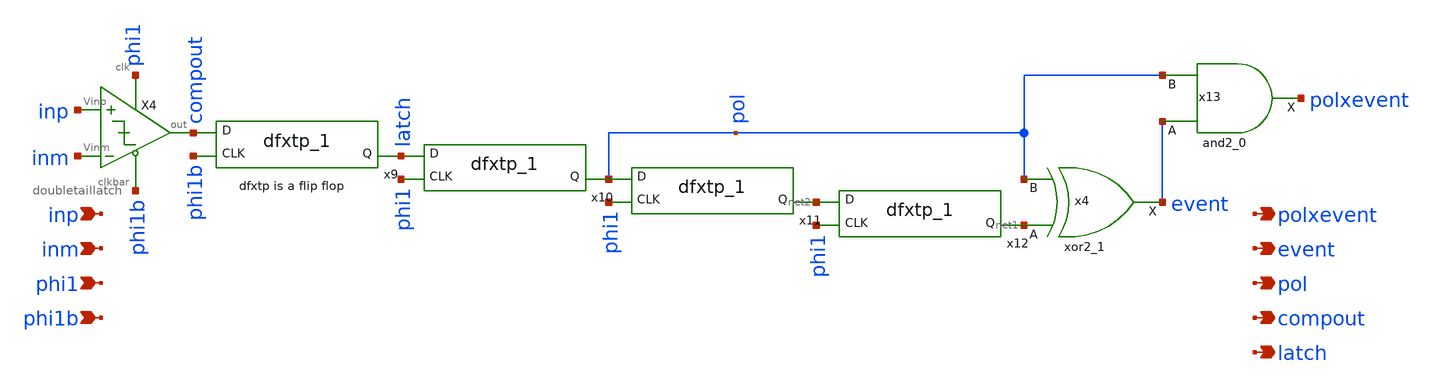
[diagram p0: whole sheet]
** sch_path: xschem/comparator/comparator_out.sch
**.subckt comparator_out inp event polxevent pol inm phi1 phi1b compout latch
*.ipin inp
*.opin event
*.opin polxevent
*.opin pol
*.ipin inm
*.ipin phi1
*.ipin phi1b
*.opin compout
*.opin latch
X4 inp inm compout phi1 phi1b doubletaillatch
x4 net1 pol GND GND VDD VDD event sky130_fd_sc_lp__xor2_1
x11 phi1 pol gnd gnd vdd vdd net2 sky130_fd_sc_lp__dfxtp_1
x12 phi1 net2 gnd gnd vdd vdd net1 sky130_fd_sc_lp__dfxtp_1
x9 phi1b compout gnd gnd vdd vdd latch sky130_fd_sc_lp__dfxtp_1
x10 phi1 latch gnd gnd vdd vdd pol sky130_fd_sc_lp__dfxtp_1
x13 event pol GND GND VDD VDD polxevent sky130_fd_sc_lp__and2_0
**.ends

* expanding   symbol:  comparator/doubletaillatch.sym # of pins=5
** sym_path: xschem/comparator/doubletaillatch.sym
** sch_path: xschem/comparator/doubletaillatch.sch
.subckt doubletaillatch Vinp Vinm out clk clkbar
*.ipin clkbar
*.opin out
*.ipin Vinp
*.ipin Vinm
*.ipin clk
XM3 rightSD out VDD VDD sky130_fd_pr__pfet_01v8 L=0.18 W=0.42 nf=1 ad='int((nf+1)/2) * W/nf * 0.29' as='int((nf+2)/2) * W/nf * 0.29'
+ pd='2*int((nf+1)/2) * (W/nf + 0.29)' ps='2*int((nf+2)/2) * (W/nf + 0.29)' nrd='0.29 / W' nrs='0.29 / W'
+ sa=0 sb=0 sd=0 mult=1 m=1
XM4 out2 rightGSD rightSD VDD sky130_fd_pr__pfet_01v8 L=0.18 W=0.42 nf=1 ad='int((nf+1)/2) * W/nf * 0.29'
+ as='int((nf+2)/2) * W/nf * 0.29' pd='2*int((nf+1)/2) * (W/nf + 0.29)' ps='2*int((nf+2)/2) * (W/nf + 0.29)'
+ nrd='0.29 / W' nrs='0.29 / W' sa=0 sb=0 sd=0 mult=1 m=1
XM5 VDD out2 leftSD VDD sky130_fd_pr__pfet_01v8 L=0.18 W=0.42 nf=1 ad='int((nf+1)/2) * W/nf * 0.29' as='int((nf+2)/2) * W/nf * 0.29'
+ pd='2*int((nf+1)/2) * (W/nf + 0.29)' ps='2*int((nf+2)/2) * (W/nf + 0.29)' nrd='0.29 / W' nrs='0.29 / W'
+ sa=0 sb=0 sd=0 mult=1 m=1
XM6 leftSD leftGD out VDD sky130_fd_pr__pfet_01v8 L=0.18 W=0.42 nf=1 ad='int((nf+1)/2) * W/nf * 0.29'
+ as='int((nf+2)/2) * W/nf * 0.29' pd='2*int((nf+1)/2) * (W/nf + 0.29)' ps='2*int((nf+2)/2) * (W/nf + 0.29)'
+ nrd='0.29 / W' nrs='0.29 / W' sa=0 sb=0 sd=0 mult=1 m=1
XM11 VDD clk rightGSD VDD sky130_fd_pr__pfet_01v8 L=0.18 W=0.42 nf=1 ad='int((nf+1)/2) * W/nf * 0.29'
+ as='int((nf+2)/2) * W/nf * 0.29' pd='2*int((nf+1)/2) * (W/nf + 0.29)' ps='2*int((nf+2)/2) * (W/nf + 0.29)'
+ nrd='0.29 / W' nrs='0.29 / W' sa=0 sb=0 sd=0 mult=1 m=1
XM12 leftGD clk VDD VDD sky130_fd_pr__pfet_01v8 L=0.18 W=0.42 nf=1 ad='int((nf+1)/2) * W/nf * 0.29' as='int((nf+2)/2) * W/nf * 0.29'
+ pd='2*int((nf+1)/2) * (W/nf + 0.29)' ps='2*int((nf+2)/2) * (W/nf + 0.29)' nrd='0.29 / W' nrs='0.29 / W'
+ sa=0 sb=0 sd=0 mult=1 m=1
XM7 out clkbar GND GND sky130_fd_pr__nfet_01v8 L=0.18 W=0.42 nf=1 ad='int((nf+1)/2) * W/nf * 0.29' as='int((nf+2)/2) * W/nf * 0.29'
+ pd='2*int((nf+1)/2) * (W/nf + 0.29)' ps='2*int((nf+2)/2) * (W/nf + 0.29)' nrd='0.29 / W' nrs='0.29 / W'
+ sa=0 sb=0 sd=0 mult=1 m=1
XM8 out2 out GND GND sky130_fd_pr__nfet_01v8 L=0.18 W=0.42 nf=1 ad='int((nf+1)/2) * W/nf * 0.29' as='int((nf+2)/2) * W/nf * 0.29'
+ pd='2*int((nf+1)/2) * (W/nf + 0.29)' ps='2*int((nf+2)/2) * (W/nf + 0.29)' nrd='0.29 / W' nrs='0.29 / W'
+ sa=0 sb=0 sd=0 mult=1 m=1
XM9 GND clkbar out2 GND sky130_fd_pr__nfet_01v8 L=0.18 W=0.42 nf=1 ad='int((nf+1)/2) * W/nf * 0.29' as='int((nf+2)/2) * W/nf * 0.29'
+ pd='2*int((nf+1)/2) * (W/nf + 0.29)' ps='2*int((nf+2)/2) * (W/nf + 0.29)' nrd='0.29 / W' nrs='0.29 / W'
+ sa=0 sb=0 sd=0 mult=1 m=1
XM10 GND out2 out GND sky130_fd_pr__nfet_01v8 L=0.18 W=0.42 nf=1 ad='int((nf+1)/2) * W/nf * 0.29' as='int((nf+2)/2) * W/nf * 0.29'
+ pd='2*int((nf+1)/2) * (W/nf + 0.29)' ps='2*int((nf+2)/2) * (W/nf + 0.29)' nrd='0.29 / W' nrs='0.29 / W'
+ sa=0 sb=0 sd=0 mult=1 m=1
XM13 leftGD Vinp rem GND sky130_fd_pr__nfet_01v8 L=0.18 W=0.42 nf=1 ad='int((nf+1)/2) * W/nf * 0.29'
+ as='int((nf+2)/2) * W/nf * 0.29' pd='2*int((nf+1)/2) * (W/nf + 0.29)' ps='2*int((nf+2)/2) * (W/nf + 0.29)'
+ nrd='0.29 / W' nrs='0.29 / W' sa=0 sb=0 sd=0 mult=1 m=1
XM14 rem Vinm rightGSD GND sky130_fd_pr__nfet_01v8 L=0.18 W=0.42 nf=1 ad='int((nf+1)/2) * W/nf * 0.29'
+ as='int((nf+2)/2) * W/nf * 0.29' pd='2*int((nf+1)/2) * (W/nf + 0.29)' ps='2*int((nf+2)/2) * (W/nf + 0.29)'
+ nrd='0.29 / W' nrs='0.29 / W' sa=0 sb=0 sd=0 mult=1 m=1
XM15 rem clk GND GND sky130_fd_pr__nfet_01v8 L=0.18 W=0.42 nf=1 ad='int((nf+1)/2) * W/nf * 0.29' as='int((nf+2)/2) * W/nf * 0.29'
+ pd='2*int((nf+1)/2) * (W/nf + 0.29)' ps='2*int((nf+2)/2) * (W/nf + 0.29)' nrd='0.29 / W' nrs='0.29 / W'
+ sa=0 sb=0 sd=0 mult=1 m=1
.ends

.GLOBAL VDD
.GLOBAL GND
.end
